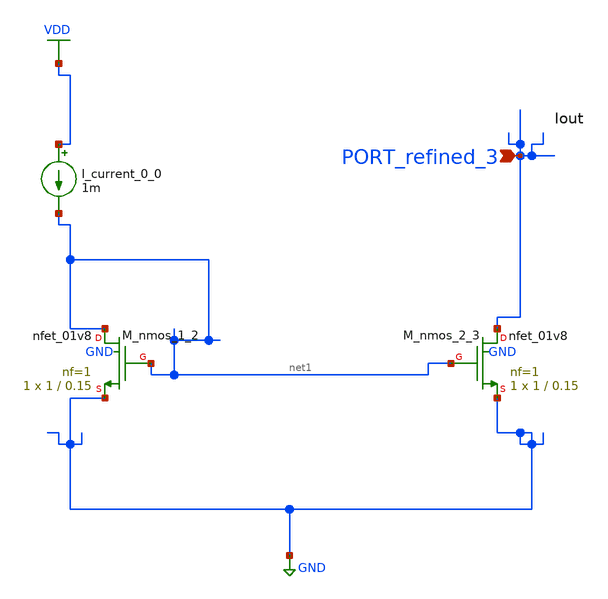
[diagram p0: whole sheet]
** sch_path: schematics/SchemGen/10_1051_epjconf_201716201048_03_001.sch
**.subckt 10_1051_epjconf_201716201048_03_001 PORT_refined_3
*.ipin PORT_refined_3
I_current_0_0 VDD net1 1m
XM_nmos_1_2 net1 net1 GND GND sky130_fd_pr__nfet_01v8 L=0.15 W=1 nf=1 ad='int((1 + 1)/2) * 1 / 1 * 0.29'
+ as='int((1 + 2)/2) * 1 / 1 * 0.29' pd='2*int((1 + 1)/2) * (1 / 1 + 0.29)' ps='2*int((1 + 2)/2) * (1 / 1 + 0.29)'
+ nrd='0.29 / 1 ' nrs='0.29 / 1 ' sa=0 sb=0 sd=0 mult=1 m=1
XM_nmos_2_3 PORT_refined_3 net1 GND GND sky130_fd_pr__nfet_01v8 L=0.15 W=1 nf=1 ad='int((1 + 1)/2) * 1 / 1 * 0.29'
+ as='int((1 + 2)/2) * 1 / 1 * 0.29' pd='2*int((1 + 1)/2) * (1 / 1 + 0.29)' ps='2*int((1 + 2)/2) * (1 / 1 + 0.29)'
+ nrd='0.29 / 1 ' nrs='0.29 / 1 ' sa=0 sb=0 sd=0 mult=1 m=1
**.ends
.GLOBAL GND
.GLOBAL VDD
.end
